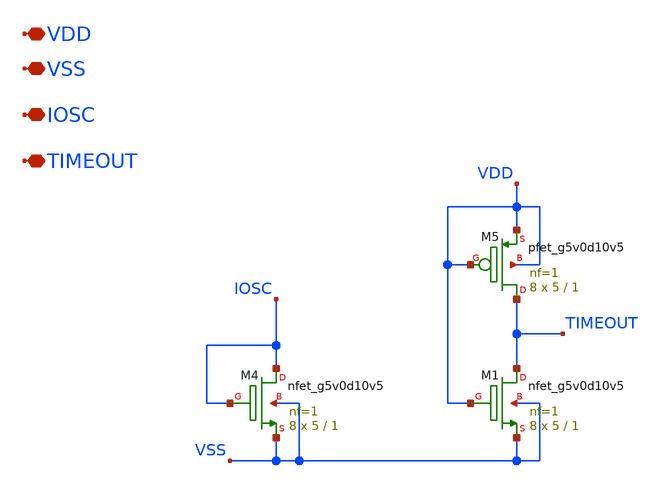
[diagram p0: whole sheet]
** sch_path: images/foss-asic-tools/addons/examples/open-pmic/design/oscillator/osc_placeholder.sch
**.subckt osc_placeholder VDD VSS IOSC TIMEOUT
*.iopin VDD
*.iopin VSS
*.iopin IOSC
*.iopin TIMEOUT
XM5 TIMEOUT VDD VDD VDD sky130_fd_pr__pfet_g5v0d10v5 L=1 W=5 nf=1 ad='int((nf+1)/2) * W/nf * 0.29' as='int((nf+2)/2) * W/nf * 0.29'
+ pd='2*int((nf+1)/2) * (W/nf + 0.29)' ps='2*int((nf+2)/2) * (W/nf + 0.29)' nrd='0.29 / W' nrs='0.29 / W'
+ sa=0 sb=0 sd=0 mult=8 m=8
XM4 IOSC IOSC VSS VSS sky130_fd_pr__nfet_g5v0d10v5 L=1 W=5 nf=1 ad='int((nf+1)/2) * W/nf * 0.29' as='int((nf+2)/2) * W/nf * 0.29'
+ pd='2*int((nf+1)/2) * (W/nf + 0.29)' ps='2*int((nf+2)/2) * (W/nf + 0.29)' nrd='0.29 / W' nrs='0.29 / W'
+ sa=0 sb=0 sd=0 mult=8 m=8
XM1 TIMEOUT VDD VSS VSS sky130_fd_pr__nfet_g5v0d10v5 L=1 W=5 nf=1 ad='int((nf+1)/2) * W/nf * 0.29' as='int((nf+2)/2) * W/nf * 0.29'
+ pd='2*int((nf+1)/2) * (W/nf + 0.29)' ps='2*int((nf+2)/2) * (W/nf + 0.29)' nrd='0.29 / W' nrs='0.29 / W'
+ sa=0 sb=0 sd=0 mult=8 m=8
**.ends
.end
